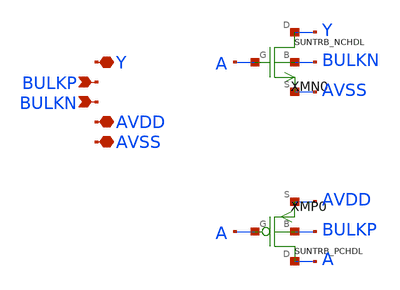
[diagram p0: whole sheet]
** sch_path: ip/sun_trb_sky130nm/design/SUN_TRB_SKY130NM/SUNTRB_TIEL_CV.sch
**.subckt SUNTRB_TIEL_CV Y BULKP BULKN AVDD AVSS
*.iopin Y
*.ipin BULKP
*.ipin BULKN
*.iopin AVDD
*.iopin AVSS
XMN0 Y A AVSS BULKN SUNTRB_NCHDL xoffset=0 yoffset=0 angle=0
XMP0 A A AVDD BULKP SUNTRB_PCHDL xoffset=0 yoffset=0 angle=0
**.ends
.end
